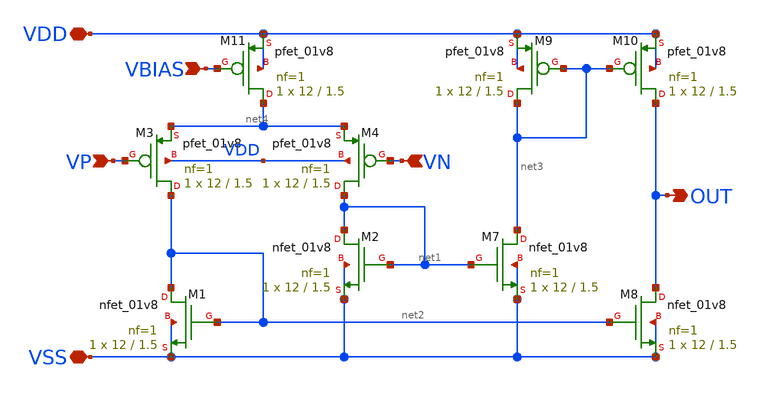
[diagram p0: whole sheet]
** sch_path: LDO_UVLO_Design/schematics/error_amplifier.sch
**.subckt error_amplifier VDD VSS VBIAS VP VN OUT
*.iopin VDD
*.iopin VSS
*.ipin VBIAS
*.ipin VP
*.ipin VN
*.opin OUT
XM1 net2 net2 VSS VSS sky130_fd_pr__nfet_01v8 L=1.5 W=12 nf=1 ad='int((nf+1)/2) * W/nf * 0.29' as='int((nf+2)/2) * W/nf * 0.29'
+ pd='2*int((nf+1)/2) * (W/nf + 0.29)' ps='2*int((nf+2)/2) * (W/nf + 0.29)' nrd='0.29 / W' nrs='0.29 / W'
+ sa=0 sb=0 sd=0 mult=1 m=1
XM2 net1 net1 VSS VSS sky130_fd_pr__nfet_01v8 L=1.5 W=12 nf=1 ad='int((nf+1)/2) * W/nf * 0.29' as='int((nf+2)/2) * W/nf * 0.29'
+ pd='2*int((nf+1)/2) * (W/nf + 0.29)' ps='2*int((nf+2)/2) * (W/nf + 0.29)' nrd='0.29 / W' nrs='0.29 / W'
+ sa=0 sb=0 sd=0 mult=1 m=1
XM3 net2 VP net4 VDD sky130_fd_pr__pfet_01v8 L=1.5 W=12 nf=1 ad='int((nf+1)/2) * W/nf * 0.29' as='int((nf+2)/2) * W/nf * 0.29'
+ pd='2*int((nf+1)/2) * (W/nf + 0.29)' ps='2*int((nf+2)/2) * (W/nf + 0.29)' nrd='0.29 / W' nrs='0.29 / W'
+ sa=0 sb=0 sd=0 mult=1 m=1
XM4 net1 VN net4 VDD sky130_fd_pr__pfet_01v8 L=1.5 W=12 nf=1 ad='int((nf+1)/2) * W/nf * 0.29' as='int((nf+2)/2) * W/nf * 0.29'
+ pd='2*int((nf+1)/2) * (W/nf + 0.29)' ps='2*int((nf+2)/2) * (W/nf + 0.29)' nrd='0.29 / W' nrs='0.29 / W'
+ sa=0 sb=0 sd=0 mult=1 m=1
XM7 net3 net1 VSS VSS sky130_fd_pr__nfet_01v8 L=1.5 W=12 nf=1 ad='int((nf+1)/2) * W/nf * 0.29' as='int((nf+2)/2) * W/nf * 0.29'
+ pd='2*int((nf+1)/2) * (W/nf + 0.29)' ps='2*int((nf+2)/2) * (W/nf + 0.29)' nrd='0.29 / W' nrs='0.29 / W'
+ sa=0 sb=0 sd=0 mult=1 m=1
XM8 OUT net2 VSS VSS sky130_fd_pr__nfet_01v8 L=1.5 W=12 nf=1 ad='int((nf+1)/2) * W/nf * 0.29' as='int((nf+2)/2) * W/nf * 0.29'
+ pd='2*int((nf+1)/2) * (W/nf + 0.29)' ps='2*int((nf+2)/2) * (W/nf + 0.29)' nrd='0.29 / W' nrs='0.29 / W'
+ sa=0 sb=0 sd=0 mult=1 m=1
XM9 net3 net3 VDD VDD sky130_fd_pr__pfet_01v8 L=1.5 W=12 nf=1 ad='int((nf+1)/2) * W/nf * 0.29' as='int((nf+2)/2) * W/nf * 0.29'
+ pd='2*int((nf+1)/2) * (W/nf + 0.29)' ps='2*int((nf+2)/2) * (W/nf + 0.29)' nrd='0.29 / W' nrs='0.29 / W'
+ sa=0 sb=0 sd=0 mult=1 m=1
XM10 OUT net3 VDD VDD sky130_fd_pr__pfet_01v8 L=1.5 W=12 nf=1 ad='int((nf+1)/2) * W/nf * 0.29' as='int((nf+2)/2) * W/nf * 0.29'
+ pd='2*int((nf+1)/2) * (W/nf + 0.29)' ps='2*int((nf+2)/2) * (W/nf + 0.29)' nrd='0.29 / W' nrs='0.29 / W'
+ sa=0 sb=0 sd=0 mult=1 m=1
XM11 net4 VBIAS VDD VDD sky130_fd_pr__pfet_01v8 L=1.5 W=12 nf=1 ad='int((nf+1)/2) * W/nf * 0.29' as='int((nf+2)/2) * W/nf * 0.29'
+ pd='2*int((nf+1)/2) * (W/nf + 0.29)' ps='2*int((nf+2)/2) * (W/nf + 0.29)' nrd='0.29 / W' nrs='0.29 / W'
+ sa=0 sb=0 sd=0 mult=1 m=1
**.ends
.end
